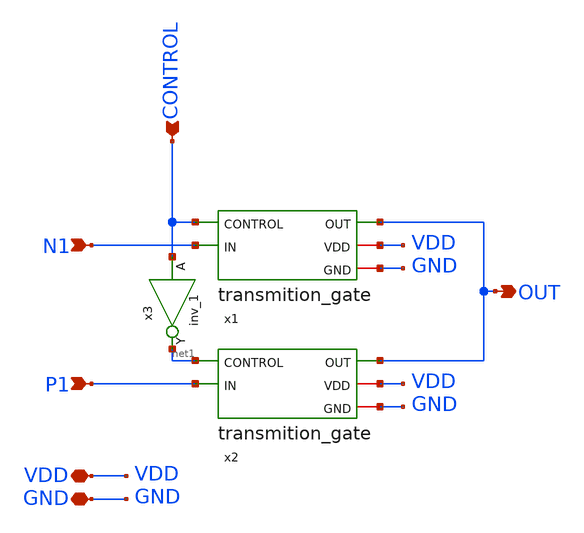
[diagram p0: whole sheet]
** sch_path: src/analog_source_files/SELECTOR.sch
**.subckt SELECTOR N1 P1 CONTROL OUT VDD GND
*.ipin N1
*.ipin P1
*.ipin CONTROL
*.opin OUT
*.iopin VDD
*.iopin GND
x1 CONTROL OUT N1 VDD GND transmition_gate
x2 net1 OUT P1 VDD GND transmition_gate
x3 CONTROL GND GND VDD VDD net1 sky130_fd_sc_hd__inv_1
**.ends

* expanding   symbol:  transmition_gate.sym # of pins=5
** sym_path: src/analog_source_files/transmition_gate.sym
** sch_path: src/analog_source_files/transmition_gate.sch
.subckt transmition_gate CONTROL OUT IN VDD GND
*.ipin IN
*.ipin CONTROL
*.opin OUT
*.iopin VDD
*.iopin GND
XM2 IN net1 OUT VDD sky130_fd_pr__pfet_01v8 L=0.15 W=1 nf=1 ad='int((1 + 1)/2) * 1 / 1 * 0.29' as='int((1 + 2)/2) * 1 / 1 * 0.29'
+ pd='2*int((1 + 1)/2) * (1 / 1 + 0.29)' ps='2*int((1 + 2)/2) * (1 / 1 + 0.29)' nrd='0.29 / 1 ' nrs='0.29 / 1 '
+ sa=0 sb=0 sd=0 mult=1 m=1
x1 CONTROL GND GND VDD VDD net1 sky130_fd_sc_hd__inv_1
XM3 IN CONTROL OUT GND sky130_fd_pr__nfet_01v8 L=0.15 W=1 nf=1 ad='int((1 + 1)/2) * 1 / 1 * 0.29' as='int((1 + 2)/2) * 1 / 1 * 0.29'
+ pd='2*int((1 + 1)/2) * (1 / 1 + 0.29)' ps='2*int((1 + 2)/2) * (1 / 1 + 0.29)' nrd='0.29 / 1 ' nrs='0.29 / 1 '
+ sa=0 sb=0 sd=0 mult=1 m=1
.ends

.end
